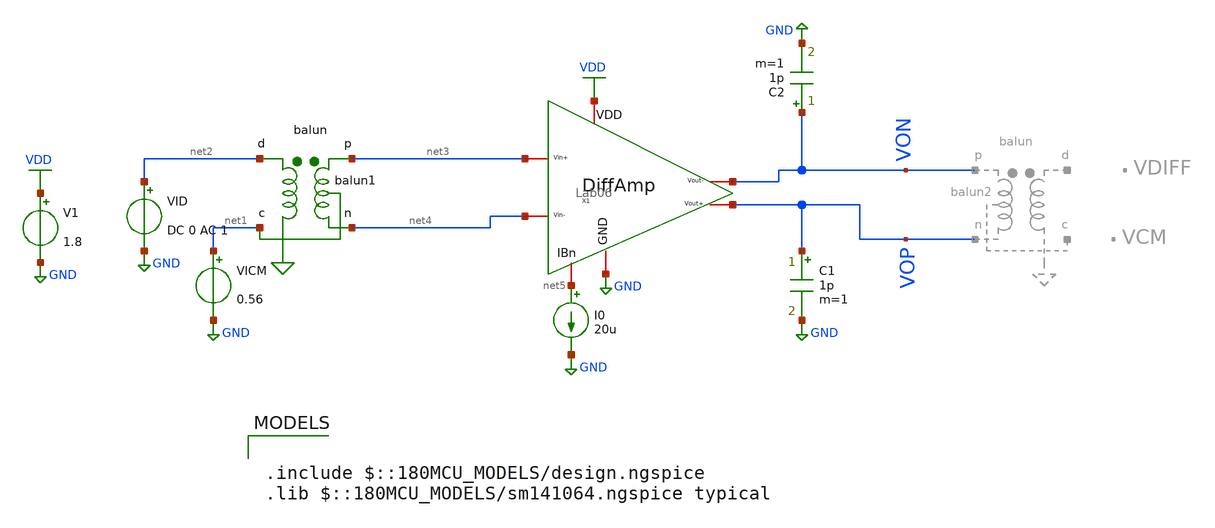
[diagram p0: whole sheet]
** sch_path: ITI_Labs/Lab7/Design/Lab06_Diff_Amp.sch
**.subckt Lab06_Diff_Amp
X1 VDD net5 net3 net4 VON VOP GND Lab06
Xbalun1 net2 net1 net3 net4 balun
V1 VDD GND 1.8
I0 net5 GND 20u
VICM net1 GND 0.56
VID net2 GND DC 0 AC 1
C1 VOP GND 1p m=1
C2 VON GND 1p m=1
**** begin user architecture code


.include sim_script.sim



.include $::180MCU_MODELS/design.ngspice
.lib $::180MCU_MODELS/sm141064.ngspice typical

**** end user architecture code
**.ends
.GLOBAL VDD
.GLOBAL GND
.end
